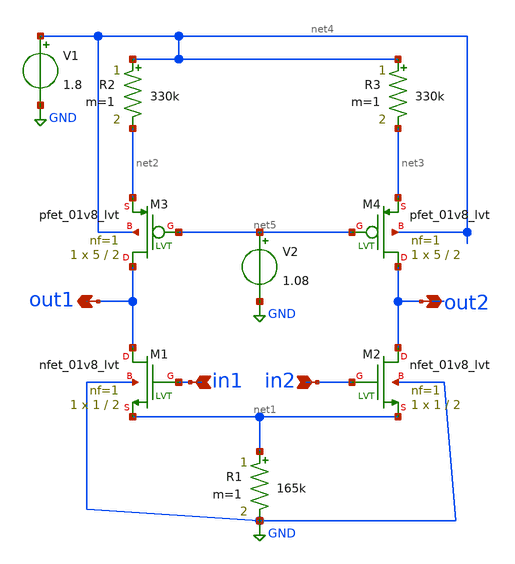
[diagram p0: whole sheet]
** sch_path: opampn.sch
**.subckt opampn in1 in2 out1 out2
*.ipin in1
*.ipin in2
*.opin out1
*.opin out2
XM1 out1 in1 net1 GND sky130_fd_pr__nfet_01v8_lvt L=2 W=1 nf=1 ad='int((nf+1)/2) * W/nf * 0.29' as='int((nf+2)/2) * W/nf * 0.29'
+ pd='2*int((nf+1)/2) * (W/nf + 0.29)' ps='2*int((nf+2)/2) * (W/nf + 0.29)' nrd='0.29 / W' nrs='0.29 / W'
+ sa=0 sb=0 sd=0 mult=1 m=1
XM2 out2 in2 net1 GND sky130_fd_pr__nfet_01v8_lvt L=2 W=1 nf=1 ad='int((nf+1)/2) * W/nf * 0.29' as='int((nf+2)/2) * W/nf * 0.29'
+ pd='2*int((nf+1)/2) * (W/nf + 0.29)' ps='2*int((nf+2)/2) * (W/nf + 0.29)' nrd='0.29 / W' nrs='0.29 / W'
+ sa=0 sb=0 sd=0 mult=1 m=1
XM3 out1 net5 net2 net4 sky130_fd_pr__pfet_01v8_lvt L=2 W=5 nf=1 ad='int((nf+1)/2) * W/nf * 0.29' as='int((nf+2)/2) * W/nf * 0.29'
+ pd='2*int((nf+1)/2) * (W/nf + 0.29)' ps='2*int((nf+2)/2) * (W/nf + 0.29)' nrd='0.29 / W' nrs='0.29 / W'
+ sa=0 sb=0 sd=0 mult=1 m=1
XM4 out2 net5 net3 net4 sky130_fd_pr__pfet_01v8_lvt L=2 W=5 nf=1 ad='int((nf+1)/2) * W/nf * 0.29' as='int((nf+2)/2) * W/nf * 0.29'
+ pd='2*int((nf+1)/2) * (W/nf + 0.29)' ps='2*int((nf+2)/2) * (W/nf + 0.29)' nrd='0.29 / W' nrs='0.29 / W'
+ sa=0 sb=0 sd=0 mult=1 m=1
R1 net1 GND 165k m=1
R2 net4 net2 330k m=1
R3 net4 net3 330k m=1
V1 net4 GND 1.8
V2 net5 GND 1.08
**.ends
.GLOBAL GND
.end
